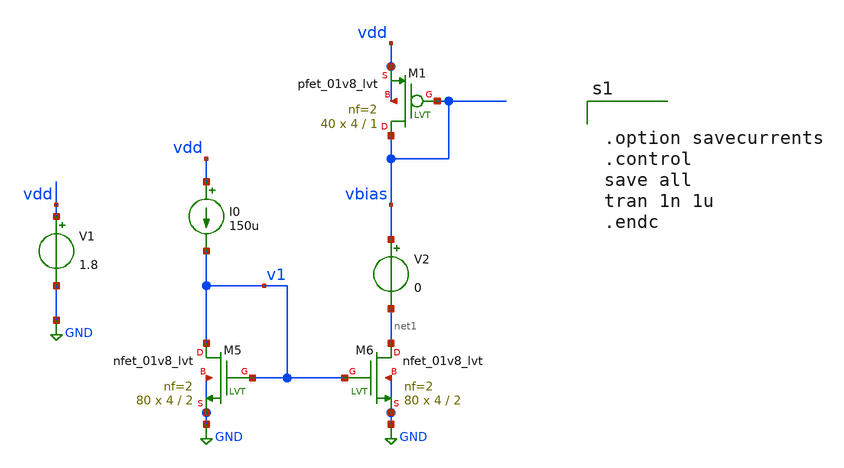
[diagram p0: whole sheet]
** sch_path: xschem/src/current_source/current_source_tb.sch
**.subckt current_source_tb
I0 vdd v1 150u
XM5 v1 v1 GND GND sky130_fd_pr__nfet_01v8_lvt L=2 W=4 nf=2 ad='int((nf+1)/2) * W/nf * 0.29' as='int((nf+2)/2) * W/nf * 0.29'
+ pd='2*int((nf+1)/2) * (W/nf + 0.29)' ps='2*int((nf+2)/2) * (W/nf + 0.29)' nrd='0.29 / W' nrs='0.29 / W'
+ sa=0 sb=0 sd=0 mult=80 m=80
XM6 net1 v1 GND GND sky130_fd_pr__nfet_01v8_lvt L=2 W=4 nf=2 ad='int((nf+1)/2) * W/nf * 0.29' as='int((nf+2)/2) * W/nf * 0.29'
+ pd='2*int((nf+1)/2) * (W/nf + 0.29)' ps='2*int((nf+2)/2) * (W/nf + 0.29)' nrd='0.29 / W' nrs='0.29 / W'
+ sa=0 sb=0 sd=0 mult=80 m=80
XM1 vbias vbias vdd vdd sky130_fd_pr__pfet_01v8_lvt L=1 W=4 nf=2 ad='int((nf+1)/2) * W/nf * 0.29' as='int((nf+2)/2) * W/nf * 0.29'
+ pd='2*int((nf+1)/2) * (W/nf + 0.29)' ps='2*int((nf+2)/2) * (W/nf + 0.29)' nrd='0.29 / W' nrs='0.29 / W'
+ sa=0 sb=0 sd=0 mult=40 m=40
V1 vdd GND 1.8
V2 vbias net1 0
**** begin user architecture code

.include /home/eda/pdk/skywater-pdk/libraries/sky130_fd_pr_ngspice/latest/models/corners/tt.spice
* Resistor$::SKYWATER_MODELS/Capacitor
.include $::SKYWATER_MODELS/models/r+c/res_typical__cap_typical.spice
.include $::SKYWATER_MODELS/models/r+c/res_typical__cap_typical__lin.spice
* Special cells
.include $::SKYWATER_MODELS/models/corners/tt/specialized_cells.spice




.option savecurrents
.control
save all
tran 1n 1u
.endc




**** end user architecture code
**.ends
.GLOBAL GND
.end
